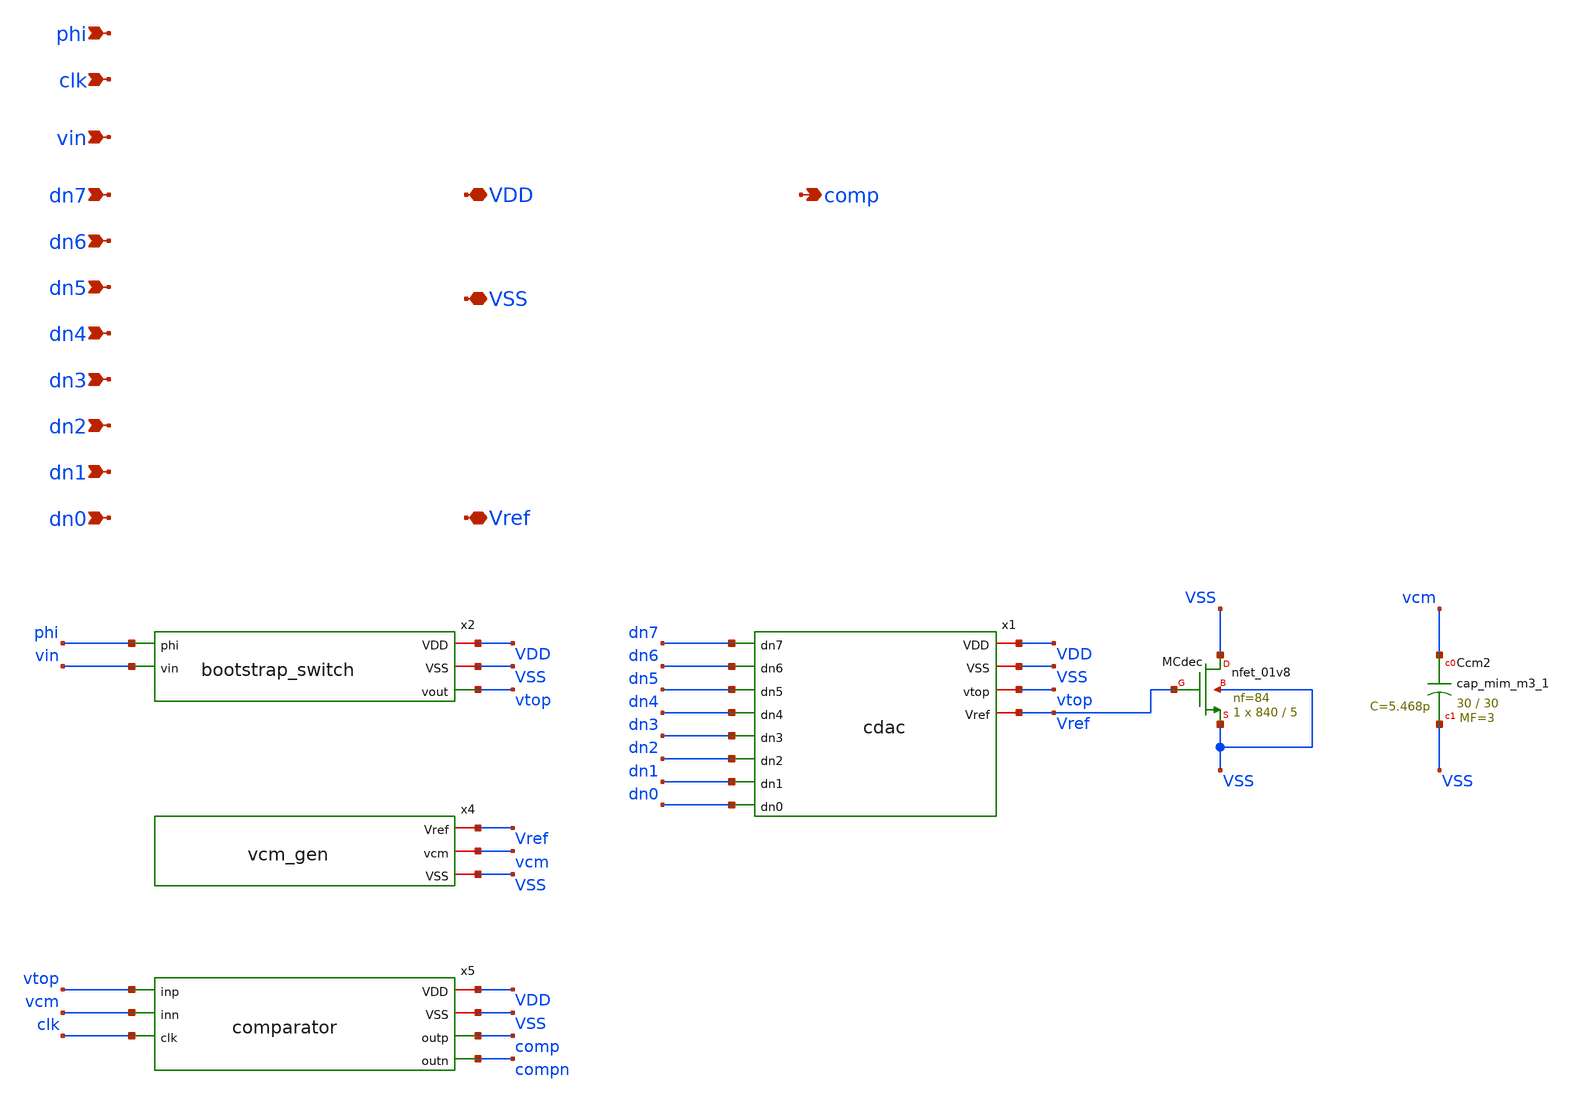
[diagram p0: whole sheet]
** sch_path: xschem/adc_core.sch
**.subckt adc_core dn7 dn6 dn5 dn4 dn3 dn2 dn1 dn0 VDD VSS Vref comp phi clk vin
*.ipin dn7
*.ipin dn6
*.ipin dn5
*.ipin dn4
*.ipin dn3
*.ipin dn2
*.ipin dn1
*.ipin dn0
*.iopin VDD
*.iopin VSS
*.iopin Vref
*.opin comp
*.ipin phi
*.ipin clk
*.ipin vin
x2 phi VDD VSS vin vtop bootstrap_switch
x4 Vref vcm VSS vcm_gen
x1 VDD dn7 dn6 dn5 VSS dn4 dn3 vtop dn2 dn1 Vref dn0 cdac
x5 vtop VDD vcm clk VSS comp compn comparator
XMCdec VSS Vref VSS VSS sky130_fd_pr__nfet_01v8 L=5 W=840 nf=84 ad='int((84 + 1)/2) * 840 / 84 * 0.29'
+ as='int((84 + 2)/2) * 840 / 84 * 0.29' pd='2*int((84 + 1)/2) * (840 / 84 + 0.29)' ps='2*int((84 + 2)/2) * (840 / 84 + 0.29)'
+ nrd='0.29 / 840 ' nrs='0.29 / 840 ' sa=0 sb=0 sd=0 mult=1 m=1
XCcm2 vcm VSS sky130_fd_pr__cap_mim_m3_1 W=30 L=30 MF=3 m=3
**.ends

* expanding   symbol:  bootstrap_switch.sym # of pins=5
** sym_path: xschem/bootstrap_switch.sym
** sch_path: xschem/bootstrap_switch.sch
.subckt bootstrap_switch phi VDD VSS vin vout
*.iopin VDD
*.iopin VSS
*.opin vout
*.ipin phi
*.ipin vin
XM8 X N P P sky130_fd_pr__pfet_01v8 L=0.15 W=2 nf=1 ad='int((1 + 1)/2) * 2 / 1 * 0.29' as='int((1 + 2)/2) * 2 / 1 * 0.29'
+ pd='2*int((1 + 1)/2) * (2 / 1 + 0.29)' ps='2*int((1 + 2)/2) * (2 / 1 + 0.29)' nrd='0.29 / 2 ' nrs='0.29 / 2 '
+ sa=0 sb=0 sd=0 mult=1 m=1
XM11 vin X vout VSS sky130_fd_pr__nfet_01v8 L=0.15 W=1 nf=1 ad='int((1 + 1)/2) * 1 / 1 * 0.29' as='int((1 + 2)/2) * 1 / 1 * 0.29'
+ pd='2*int((1 + 1)/2) * (1 / 1 + 0.29)' ps='2*int((1 + 2)/2) * (1 / 1 + 0.29)' nrd='0.29 / 1 ' nrs='0.29 / 1 '
+ sa=0 sb=0 sd=0 mult=1 m=1
XC2 P B sky130_fd_pr__cap_mim_m3_1 W=11 L=11 MF=2 m=2
XM9 B X vin VSS sky130_fd_pr__nfet_01v8 L=0.15 W=2 nf=1 ad='int((1 + 1)/2) * 2 / 1 * 0.29' as='int((1 + 2)/2) * 2 / 1 * 0.29'
+ pd='2*int((1 + 1)/2) * (2 / 1 + 0.29)' ps='2*int((1 + 2)/2) * (2 / 1 + 0.29)' nrd='0.29 / 2 ' nrs='0.29 / 2 '
+ sa=0 sb=0 sd=0 mult=1 m=1
XM12 VSS phi_b B VSS sky130_fd_pr__nfet_01v8 L=0.15 W=1 nf=1 ad='int((1 + 1)/2) * 1 / 1 * 0.29' as='int((1 + 2)/2) * 1 / 1 * 0.29'
+ pd='2*int((1 + 1)/2) * (1 / 1 + 0.29)' ps='2*int((1 + 2)/2) * (1 / 1 + 0.29)' nrd='0.29 / 1 ' nrs='0.29 / 1 '
+ sa=0 sb=0 sd=0 mult=1 m=1
XM14 X VDD net1 VSS sky130_fd_pr__nfet_01v8 L=0.15 W=4 nf=1 ad='int((1 + 1)/2) * 4 / 1 * 0.29' as='int((1 + 2)/2) * 4 / 1 * 0.29'
+ pd='2*int((1 + 1)/2) * (4 / 1 + 0.29)' ps='2*int((1 + 2)/2) * (4 / 1 + 0.29)' nrd='0.29 / 4 ' nrs='0.29 / 4 '
+ sa=0 sb=0 sd=0 mult=1 m=1
XM3 P X VDD P sky130_fd_pr__pfet_01v8 L=0.15 W=2 nf=1 ad='int((1 + 1)/2) * 2 / 1 * 0.29' as='int((1 + 2)/2) * 2 / 1 * 0.29'
+ pd='2*int((1 + 1)/2) * (2 / 1 + 0.29)' ps='2*int((1 + 2)/2) * (2 / 1 + 0.29)' nrd='0.29 / 2 ' nrs='0.29 / 2 '
+ sa=0 sb=0 sd=0 mult=1 m=1
XM10 net1 phi_b VSS VSS sky130_fd_pr__nfet_01v8 L=0.15 W=1 nf=1 ad='int((1 + 1)/2) * 1 / 1 * 0.29' as='int((1 + 2)/2) * 1 / 1 * 0.29'
+ pd='2*int((1 + 1)/2) * (1 / 1 + 0.29)' ps='2*int((1 + 2)/2) * (1 / 1 + 0.29)' nrd='0.29 / 1 ' nrs='0.29 / 1 '
+ sa=0 sb=0 sd=0 mult=1 m=1
XM15 N phi B VSS sky130_fd_pr__nfet_01v8 L=0.15 W=1 nf=1 ad='int((1 + 1)/2) * 1 / 1 * 0.29' as='int((1 + 2)/2) * 1 / 1 * 0.29'
+ pd='2*int((1 + 1)/2) * (1 / 1 + 0.29)' ps='2*int((1 + 2)/2) * (1 / 1 + 0.29)' nrd='0.29 / 1 ' nrs='0.29 / 1 '
+ sa=0 sb=0 sd=0 mult=1 m=1
XM16 N phi VDD VDD sky130_fd_pr__pfet_01v8 L=0.15 W=1 nf=1 ad='int((1 + 1)/2) * 1 / 1 * 0.29' as='int((1 + 2)/2) * 1 / 1 * 0.29'
+ pd='2*int((1 + 1)/2) * (1 / 1 + 0.29)' ps='2*int((1 + 2)/2) * (1 / 1 + 0.29)' nrd='0.29 / 1 ' nrs='0.29 / 1 '
+ sa=0 sb=0 sd=0 mult=1 m=1
XMIN phi_b phi VSS VSS sky130_fd_pr__nfet_01v8 L=0.15 W=1 nf=1 ad='int((1 + 1)/2) * 1 / 1 * 0.29' as='int((1 + 2)/2) * 1 / 1 * 0.29'
+ pd='2*int((1 + 1)/2) * (1 / 1 + 0.29)' ps='2*int((1 + 2)/2) * (1 / 1 + 0.29)' nrd='0.29 / 1 ' nrs='0.29 / 1 '
+ sa=0 sb=0 sd=0 mult=1 m=1
XMIP phi_b phi VDD VDD sky130_fd_pr__pfet_01v8 L=0.15 W=2 nf=1 ad='int((1 + 1)/2) * 2 / 1 * 0.29' as='int((1 + 2)/2) * 2 / 1 * 0.29'
+ pd='2*int((1 + 1)/2) * (2 / 1 + 0.29)' ps='2*int((1 + 2)/2) * (2 / 1 + 0.29)' nrd='0.29 / 2 ' nrs='0.29 / 2 '
+ sa=0 sb=0 sd=0 mult=1 m=1
.ends


* expanding   symbol:  vcm_gen.sym # of pins=3
** sym_path: xschem/vcm_gen.sym
** sch_path: xschem/vcm_gen.sch
.subckt vcm_gen Vref vcm VSS
*.iopin Vref
*.iopin vcm
*.iopin VSS
XR1 vcm Vref VSS sky130_fd_pr__res_xhigh_po_0p35 L=9 mult=1 m=1
XR2 VSS vcm VSS sky130_fd_pr__res_xhigh_po_0p35 L=9 mult=1 m=1
XCcm vcm VSS sky130_fd_pr__cap_mim_m3_1 W=22 L=22 MF=2 m=2
.ends


* expanding   symbol:  cdac.sym # of pins=12
** sym_path: xschem/cdac.sym
** sch_path: xschem/cdac.sch
.subckt cdac VDD dn7 dn6 dn5 VSS dn4 dn3 vtop dn2 dn1 Vref dn0
*.ipin dn7
*.ipin dn6
*.ipin dn5
*.ipin dn4
*.ipin dn3
*.ipin dn2
*.ipin dn1
*.ipin dn0
*.iopin VDD
*.iopin VSS
*.iopin vtop
*.iopin Vref
XMN7 b7 dn7 VSS VSS sky130_fd_pr__nfet_01v8 L=0.15 W=16 nf=4 ad='int((4 + 1)/2) * 16 / 4 * 0.29' as='int((4 + 2)/2) * 16 / 4 * 0.29'
+ pd='2*int((4 + 1)/2) * (16 / 4 + 0.29)' ps='2*int((4 + 2)/2) * (16 / 4 + 0.29)' nrd='0.29 / 16 ' nrs='0.29 / 16 '
+ sa=0 sb=0 sd=0 mult=1 m=1
XMP7 b7 dn7 Vref Vref sky130_fd_pr__pfet_01v8_lvt L=0.35 W=32 nf=8 ad='int((8 + 1)/2) * 32 / 8 * 0.29'
+ as='int((8 + 2)/2) * 32 / 8 * 0.29' pd='2*int((8 + 1)/2) * (32 / 8 + 0.29)' ps='2*int((8 + 2)/2) * (32 / 8 + 0.29)'
+ nrd='0.29 / 32 ' nrs='0.29 / 32 ' sa=0 sb=0 sd=0 mult=1 m=1
XC7 vtop b7 sky130_fd_pr__cap_mim_m3_1 W=1.8 L=1.8 MF=128 m=128
XMN6 b6 dn6 VSS VSS sky130_fd_pr__nfet_01v8 L=0.15 W=8 nf=2 ad='int((2 + 1)/2) * 8 / 2 * 0.29' as='int((2 + 2)/2) * 8 / 2 * 0.29'
+ pd='2*int((2 + 1)/2) * (8 / 2 + 0.29)' ps='2*int((2 + 2)/2) * (8 / 2 + 0.29)' nrd='0.29 / 8 ' nrs='0.29 / 8 '
+ sa=0 sb=0 sd=0 mult=1 m=1
XMP6 b6 dn6 Vref Vref sky130_fd_pr__pfet_01v8_lvt L=0.35 W=16 nf=4 ad='int((4 + 1)/2) * 16 / 4 * 0.29'
+ as='int((4 + 2)/2) * 16 / 4 * 0.29' pd='2*int((4 + 1)/2) * (16 / 4 + 0.29)' ps='2*int((4 + 2)/2) * (16 / 4 + 0.29)'
+ nrd='0.29 / 16 ' nrs='0.29 / 16 ' sa=0 sb=0 sd=0 mult=1 m=1
XC6 vtop b6 sky130_fd_pr__cap_mim_m3_1 W=1.8 L=1.8 MF=64 m=64
XMN5 b5 dn5 VSS VSS sky130_fd_pr__nfet_01v8 L=0.15 W=4 nf=1 ad='int((1 + 1)/2) * 4 / 1 * 0.29' as='int((1 + 2)/2) * 4 / 1 * 0.29'
+ pd='2*int((1 + 1)/2) * (4 / 1 + 0.29)' ps='2*int((1 + 2)/2) * (4 / 1 + 0.29)' nrd='0.29 / 4 ' nrs='0.29 / 4 '
+ sa=0 sb=0 sd=0 mult=1 m=1
XMP5 b5 dn5 Vref Vref sky130_fd_pr__pfet_01v8_lvt L=0.35 W=8 nf=2 ad='int((2 + 1)/2) * 8 / 2 * 0.29'
+ as='int((2 + 2)/2) * 8 / 2 * 0.29' pd='2*int((2 + 1)/2) * (8 / 2 + 0.29)' ps='2*int((2 + 2)/2) * (8 / 2 + 0.29)'
+ nrd='0.29 / 8 ' nrs='0.29 / 8 ' sa=0 sb=0 sd=0 mult=1 m=1
XC5 vtop b5 sky130_fd_pr__cap_mim_m3_1 W=1.8 L=1.8 MF=32 m=32
XMN4 b4 dn4 VSS VSS sky130_fd_pr__nfet_01v8 L=0.15 W=2 nf=1 ad='int((1 + 1)/2) * 2 / 1 * 0.29' as='int((1 + 2)/2) * 2 / 1 * 0.29'
+ pd='2*int((1 + 1)/2) * (2 / 1 + 0.29)' ps='2*int((1 + 2)/2) * (2 / 1 + 0.29)' nrd='0.29 / 2 ' nrs='0.29 / 2 '
+ sa=0 sb=0 sd=0 mult=1 m=1
XMP4 b4 dn4 Vref Vref sky130_fd_pr__pfet_01v8_lvt L=0.35 W=4 nf=1 ad='int((1 + 1)/2) * 4 / 1 * 0.29'
+ as='int((1 + 2)/2) * 4 / 1 * 0.29' pd='2*int((1 + 1)/2) * (4 / 1 + 0.29)' ps='2*int((1 + 2)/2) * (4 / 1 + 0.29)'
+ nrd='0.29 / 4 ' nrs='0.29 / 4 ' sa=0 sb=0 sd=0 mult=1 m=1
XC4 vtop b4 sky130_fd_pr__cap_mim_m3_1 W=1.8 L=1.8 MF=16 m=16
XMN3 b3 dn3 VSS VSS sky130_fd_pr__nfet_01v8 L=0.15 W=0.5 nf=1 ad='int((1 + 1)/2) * 0.5 / 1 * 0.29' as='int((1 + 2)/2) * 0.5 / 1 * 0.29'
+ pd='2*int((1 + 1)/2) * (0.5 / 1 + 0.29)' ps='2*int((1 + 2)/2) * (0.5 / 1 + 0.29)' nrd='0.29 / 0.5 ' nrs='0.29 / 0.5 '
+ sa=0 sb=0 sd=0 mult=1 m=1
XMP3 b3 dn3 Vref Vref sky130_fd_pr__pfet_01v8_lvt L=0.35 W=1 nf=1 ad='int((1 + 1)/2) * 1 / 1 * 0.29'
+ as='int((1 + 2)/2) * 1 / 1 * 0.29' pd='2*int((1 + 1)/2) * (1 / 1 + 0.29)' ps='2*int((1 + 2)/2) * (1 / 1 + 0.29)'
+ nrd='0.29 / 1 ' nrs='0.29 / 1 ' sa=0 sb=0 sd=0 mult=1 m=1
XC3 vtop b3 sky130_fd_pr__cap_mim_m3_1 W=1.8 L=1.8 MF=8 m=8
XMN2 b2 dn2 VSS VSS sky130_fd_pr__nfet_01v8 L=0.15 W=0.5 nf=1 ad='int((1 + 1)/2) * 0.5 / 1 * 0.29' as='int((1 + 2)/2) * 0.5 / 1 * 0.29'
+ pd='2*int((1 + 1)/2) * (0.5 / 1 + 0.29)' ps='2*int((1 + 2)/2) * (0.5 / 1 + 0.29)' nrd='0.29 / 0.5 ' nrs='0.29 / 0.5 '
+ sa=0 sb=0 sd=0 mult=1 m=1
XMP2 b2 dn2 Vref Vref sky130_fd_pr__pfet_01v8_lvt L=0.35 W=1 nf=1 ad='int((1 + 1)/2) * 1 / 1 * 0.29'
+ as='int((1 + 2)/2) * 1 / 1 * 0.29' pd='2*int((1 + 1)/2) * (1 / 1 + 0.29)' ps='2*int((1 + 2)/2) * (1 / 1 + 0.29)'
+ nrd='0.29 / 1 ' nrs='0.29 / 1 ' sa=0 sb=0 sd=0 mult=1 m=1
XC2 vtop b2 sky130_fd_pr__cap_mim_m3_1 W=1.8 L=1.8 MF=4 m=4
XMN1 b1 dn1 VSS VSS sky130_fd_pr__nfet_01v8 L=0.15 W=0.5 nf=1 ad='int((1 + 1)/2) * 0.5 / 1 * 0.29' as='int((1 + 2)/2) * 0.5 / 1 * 0.29'
+ pd='2*int((1 + 1)/2) * (0.5 / 1 + 0.29)' ps='2*int((1 + 2)/2) * (0.5 / 1 + 0.29)' nrd='0.29 / 0.5 ' nrs='0.29 / 0.5 '
+ sa=0 sb=0 sd=0 mult=1 m=1
XMP1 b1 dn1 Vref Vref sky130_fd_pr__pfet_01v8_lvt L=0.35 W=1 nf=1 ad='int((1 + 1)/2) * 1 / 1 * 0.29'
+ as='int((1 + 2)/2) * 1 / 1 * 0.29' pd='2*int((1 + 1)/2) * (1 / 1 + 0.29)' ps='2*int((1 + 2)/2) * (1 / 1 + 0.29)'
+ nrd='0.29 / 1 ' nrs='0.29 / 1 ' sa=0 sb=0 sd=0 mult=1 m=1
XC1 vtop b1 sky130_fd_pr__cap_mim_m3_1 W=1.8 L=1.8 MF=2 m=2
XMN0 b0 dn0 VSS VSS sky130_fd_pr__nfet_01v8 L=0.15 W=0.5 nf=1 ad='int((1 + 1)/2) * 0.5 / 1 * 0.29' as='int((1 + 2)/2) * 0.5 / 1 * 0.29'
+ pd='2*int((1 + 1)/2) * (0.5 / 1 + 0.29)' ps='2*int((1 + 2)/2) * (0.5 / 1 + 0.29)' nrd='0.29 / 0.5 ' nrs='0.29 / 0.5 '
+ sa=0 sb=0 sd=0 mult=1 m=1
XMP0 b0 dn0 Vref Vref sky130_fd_pr__pfet_01v8_lvt L=0.35 W=1 nf=1 ad='int((1 + 1)/2) * 1 / 1 * 0.29'
+ as='int((1 + 2)/2) * 1 / 1 * 0.29' pd='2*int((1 + 1)/2) * (1 / 1 + 0.29)' ps='2*int((1 + 2)/2) * (1 / 1 + 0.29)'
+ nrd='0.29 / 1 ' nrs='0.29 / 1 ' sa=0 sb=0 sd=0 mult=1 m=1
XC0 vtop b0 sky130_fd_pr__cap_mim_m3_1 W=1.8 L=1.8 MF=1 m=1
XCdmy vtop VSS sky130_fd_pr__cap_mim_m3_1 W=1.8 L=1.8 MF=1 m=1
.ends


* expanding   symbol:  comparator.sym # of pins=7
** sym_path: xschem/comparator.sym
** sch_path: xschem/comparator.sch
.subckt comparator inp VDD inn clk VSS outp outn
*.ipin inp
*.ipin inn
*.ipin clk
*.opin outp
*.opin outn
*.iopin VDD
*.iopin VSS
x1 inp VDD inn clk VSS X Y comparator_sa
XMI1N Yb Y VSS VSS sky130_fd_pr__nfet_01v8 L=0.15 W=1 nf=1 ad='int((1 + 1)/2) * 1 / 1 * 0.29' as='int((1 + 2)/2) * 1 / 1 * 0.29'
+ pd='2*int((1 + 1)/2) * (1 / 1 + 0.29)' ps='2*int((1 + 2)/2) * (1 / 1 + 0.29)' nrd='0.29 / 1 ' nrs='0.29 / 1 '
+ sa=0 sb=0 sd=0 mult=1 m=1
XMI1P Yb Y VDD VDD sky130_fd_pr__pfet_01v8 L=0.15 W=2 nf=1 ad='int((1 + 1)/2) * 2 / 1 * 0.29' as='int((1 + 2)/2) * 2 / 1 * 0.29'
+ pd='2*int((1 + 1)/2) * (2 / 1 + 0.29)' ps='2*int((1 + 2)/2) * (2 / 1 + 0.29)' nrd='0.29 / 2 ' nrs='0.29 / 2 '
+ sa=0 sb=0 sd=0 mult=1 m=1
XMI2N Xb X VSS VSS sky130_fd_pr__nfet_01v8 L=0.15 W=1 nf=1 ad='int((1 + 1)/2) * 1 / 1 * 0.29' as='int((1 + 2)/2) * 1 / 1 * 0.29'
+ pd='2*int((1 + 1)/2) * (1 / 1 + 0.29)' ps='2*int((1 + 2)/2) * (1 / 1 + 0.29)' nrd='0.29 / 1 ' nrs='0.29 / 1 '
+ sa=0 sb=0 sd=0 mult=1 m=1
XMI2P Xb X VDD VDD sky130_fd_pr__pfet_01v8 L=0.15 W=2 nf=1 ad='int((1 + 1)/2) * 2 / 1 * 0.29' as='int((1 + 2)/2) * 2 / 1 * 0.29'
+ pd='2*int((1 + 1)/2) * (2 / 1 + 0.29)' ps='2*int((1 + 2)/2) * (2 / 1 + 0.29)' nrd='0.29 / 2 ' nrs='0.29 / 2 '
+ sa=0 sb=0 sd=0 mult=1 m=1
XMA1 outp Yb VDD VDD sky130_fd_pr__pfet_01v8 L=0.15 W=1 nf=1 ad='int((1 + 1)/2) * 1 / 1 * 0.29' as='int((1 + 2)/2) * 1 / 1 * 0.29'
+ pd='2*int((1 + 1)/2) * (1 / 1 + 0.29)' ps='2*int((1 + 2)/2) * (1 / 1 + 0.29)' nrd='0.29 / 1 ' nrs='0.29 / 1 '
+ sa=0 sb=0 sd=0 mult=1 m=1
XMA2 outp outn VDD VDD sky130_fd_pr__pfet_01v8 L=0.15 W=1 nf=1 ad='int((1 + 1)/2) * 1 / 1 * 0.29' as='int((1 + 2)/2) * 1 / 1 * 0.29'
+ pd='2*int((1 + 1)/2) * (1 / 1 + 0.29)' ps='2*int((1 + 2)/2) * (1 / 1 + 0.29)' nrd='0.29 / 1 ' nrs='0.29 / 1 '
+ sa=0 sb=0 sd=0 mult=1 m=1
XMA3 outp Yb na VSS sky130_fd_pr__nfet_01v8 L=0.15 W=2 nf=1 ad='int((1 + 1)/2) * 2 / 1 * 0.29' as='int((1 + 2)/2) * 2 / 1 * 0.29'
+ pd='2*int((1 + 1)/2) * (2 / 1 + 0.29)' ps='2*int((1 + 2)/2) * (2 / 1 + 0.29)' nrd='0.29 / 2 ' nrs='0.29 / 2 '
+ sa=0 sb=0 sd=0 mult=1 m=1
XMA4 na outn VSS VSS sky130_fd_pr__nfet_01v8 L=0.15 W=2 nf=1 ad='int((1 + 1)/2) * 2 / 1 * 0.29' as='int((1 + 2)/2) * 2 / 1 * 0.29'
+ pd='2*int((1 + 1)/2) * (2 / 1 + 0.29)' ps='2*int((1 + 2)/2) * (2 / 1 + 0.29)' nrd='0.29 / 2 ' nrs='0.29 / 2 '
+ sa=0 sb=0 sd=0 mult=1 m=1
XMB1 outn Xb VDD VDD sky130_fd_pr__pfet_01v8 L=0.15 W=1 nf=1 ad='int((1 + 1)/2) * 1 / 1 * 0.29' as='int((1 + 2)/2) * 1 / 1 * 0.29'
+ pd='2*int((1 + 1)/2) * (1 / 1 + 0.29)' ps='2*int((1 + 2)/2) * (1 / 1 + 0.29)' nrd='0.29 / 1 ' nrs='0.29 / 1 '
+ sa=0 sb=0 sd=0 mult=1 m=1
XMB2 outn outp VDD VDD sky130_fd_pr__pfet_01v8 L=0.15 W=1 nf=1 ad='int((1 + 1)/2) * 1 / 1 * 0.29' as='int((1 + 2)/2) * 1 / 1 * 0.29'
+ pd='2*int((1 + 1)/2) * (1 / 1 + 0.29)' ps='2*int((1 + 2)/2) * (1 / 1 + 0.29)' nrd='0.29 / 1 ' nrs='0.29 / 1 '
+ sa=0 sb=0 sd=0 mult=1 m=1
XMB3 outn Xb nb VSS sky130_fd_pr__nfet_01v8 L=0.15 W=2 nf=1 ad='int((1 + 1)/2) * 2 / 1 * 0.29' as='int((1 + 2)/2) * 2 / 1 * 0.29'
+ pd='2*int((1 + 1)/2) * (2 / 1 + 0.29)' ps='2*int((1 + 2)/2) * (2 / 1 + 0.29)' nrd='0.29 / 2 ' nrs='0.29 / 2 '
+ sa=0 sb=0 sd=0 mult=1 m=1
XMB4 nb outp VSS VSS sky130_fd_pr__nfet_01v8 L=0.15 W=2 nf=1 ad='int((1 + 1)/2) * 2 / 1 * 0.29' as='int((1 + 2)/2) * 2 / 1 * 0.29'
+ pd='2*int((1 + 1)/2) * (2 / 1 + 0.29)' ps='2*int((1 + 2)/2) * (2 / 1 + 0.29)' nrd='0.29 / 2 ' nrs='0.29 / 2 '
+ sa=0 sb=0 sd=0 mult=1 m=1
.ends


* expanding   symbol:  comparator_sa.sym # of pins=7
** sym_path: xschem/comparator_sa.sym
** sch_path: xschem/comparator_sa.sch
.subckt comparator_sa inp VDD inn clk VSS X Y
*.ipin inp
*.ipin inn
*.ipin clk
*.opin X
*.opin Y
*.iopin VDD
*.iopin VSS
XM7 T ckb VDD VDD sky130_fd_pr__pfet_01v8 L=0.15 W=4 nf=1 ad='int((1 + 1)/2) * 4 / 1 * 0.29' as='int((1 + 2)/2) * 4 / 1 * 0.29'
+ pd='2*int((1 + 1)/2) * (4 / 1 + 0.29)' ps='2*int((1 + 2)/2) * (4 / 1 + 0.29)' nrd='0.29 / 4 ' nrs='0.29 / 4 '
+ sa=0 sb=0 sd=0 mult=1 m=1
XM1 P inp T T sky130_fd_pr__pfet_01v8 L=0.5 W=8 nf=4 ad='int((4 + 1)/2) * 8 / 4 * 0.29' as='int((4 + 2)/2) * 8 / 4 * 0.29'
+ pd='2*int((4 + 1)/2) * (8 / 4 + 0.29)' ps='2*int((4 + 2)/2) * (8 / 4 + 0.29)' nrd='0.29 / 8 ' nrs='0.29 / 8 '
+ sa=0 sb=0 sd=0 mult=1 m=1
XM2 Q inn T T sky130_fd_pr__pfet_01v8 L=0.5 W=8 nf=4 ad='int((4 + 1)/2) * 8 / 4 * 0.29' as='int((4 + 2)/2) * 8 / 4 * 0.29'
+ pd='2*int((4 + 1)/2) * (8 / 4 + 0.29)' ps='2*int((4 + 2)/2) * (8 / 4 + 0.29)' nrd='0.29 / 8 ' nrs='0.29 / 8 '
+ sa=0 sb=0 sd=0 mult=1 m=1
XM3 X Y P VDD sky130_fd_pr__pfet_01v8 L=0.15 W=2 nf=1 ad='int((1 + 1)/2) * 2 / 1 * 0.29' as='int((1 + 2)/2) * 2 / 1 * 0.29'
+ pd='2*int((1 + 1)/2) * (2 / 1 + 0.29)' ps='2*int((1 + 2)/2) * (2 / 1 + 0.29)' nrd='0.29 / 2 ' nrs='0.29 / 2 '
+ sa=0 sb=0 sd=0 mult=1 m=1
XM4 Y X Q VDD sky130_fd_pr__pfet_01v8 L=0.15 W=2 nf=1 ad='int((1 + 1)/2) * 2 / 1 * 0.29' as='int((1 + 2)/2) * 2 / 1 * 0.29'
+ pd='2*int((1 + 1)/2) * (2 / 1 + 0.29)' ps='2*int((1 + 2)/2) * (2 / 1 + 0.29)' nrd='0.29 / 2 ' nrs='0.29 / 2 '
+ sa=0 sb=0 sd=0 mult=1 m=1
XM6 Y X VSS VSS sky130_fd_pr__nfet_01v8 L=0.15 W=1 nf=1 ad='int((1 + 1)/2) * 1 / 1 * 0.29' as='int((1 + 2)/2) * 1 / 1 * 0.29'
+ pd='2*int((1 + 1)/2) * (1 / 1 + 0.29)' ps='2*int((1 + 2)/2) * (1 / 1 + 0.29)' nrd='0.29 / 1 ' nrs='0.29 / 1 '
+ sa=0 sb=0 sd=0 mult=1 m=1
XM5 X Y VSS VSS sky130_fd_pr__nfet_01v8 L=0.15 W=1 nf=1 ad='int((1 + 1)/2) * 1 / 1 * 0.29' as='int((1 + 2)/2) * 1 / 1 * 0.29'
+ pd='2*int((1 + 1)/2) * (1 / 1 + 0.29)' ps='2*int((1 + 2)/2) * (1 / 1 + 0.29)' nrd='0.29 / 1 ' nrs='0.29 / 1 '
+ sa=0 sb=0 sd=0 mult=1 m=1
XS4 Y ckb VSS VSS sky130_fd_pr__nfet_01v8 L=0.6 W=2 nf=1 ad='int((1 + 1)/2) * 2 / 1 * 0.29' as='int((1 + 2)/2) * 2 / 1 * 0.29'
+ pd='2*int((1 + 1)/2) * (2 / 1 + 0.29)' ps='2*int((1 + 2)/2) * (2 / 1 + 0.29)' nrd='0.29 / 2 ' nrs='0.29 / 2 '
+ sa=0 sb=0 sd=0 mult=1 m=1
XS2 Q ckb VSS VSS sky130_fd_pr__nfet_01v8 L=0.6 W=2 nf=1 ad='int((1 + 1)/2) * 2 / 1 * 0.29' as='int((1 + 2)/2) * 2 / 1 * 0.29'
+ pd='2*int((1 + 1)/2) * (2 / 1 + 0.29)' ps='2*int((1 + 2)/2) * (2 / 1 + 0.29)' nrd='0.29 / 2 ' nrs='0.29 / 2 '
+ sa=0 sb=0 sd=0 mult=1 m=1
XS3 X ckb VSS VSS sky130_fd_pr__nfet_01v8 L=0.6 W=2 nf=1 ad='int((1 + 1)/2) * 2 / 1 * 0.29' as='int((1 + 2)/2) * 2 / 1 * 0.29'
+ pd='2*int((1 + 1)/2) * (2 / 1 + 0.29)' ps='2*int((1 + 2)/2) * (2 / 1 + 0.29)' nrd='0.29 / 2 ' nrs='0.29 / 2 '
+ sa=0 sb=0 sd=0 mult=1 m=1
XS1 P ckb VSS VSS sky130_fd_pr__nfet_01v8 L=0.6 W=2 nf=1 ad='int((1 + 1)/2) * 2 / 1 * 0.29' as='int((1 + 2)/2) * 2 / 1 * 0.29'
+ pd='2*int((1 + 1)/2) * (2 / 1 + 0.29)' ps='2*int((1 + 2)/2) * (2 / 1 + 0.29)' nrd='0.29 / 2 ' nrs='0.29 / 2 '
+ sa=0 sb=0 sd=0 mult=1 m=1
XMIN ckb clk VSS VSS sky130_fd_pr__nfet_01v8 L=0.15 W=1 nf=1 ad='int((1 + 1)/2) * 1 / 1 * 0.29' as='int((1 + 2)/2) * 1 / 1 * 0.29'
+ pd='2*int((1 + 1)/2) * (1 / 1 + 0.29)' ps='2*int((1 + 2)/2) * (1 / 1 + 0.29)' nrd='0.29 / 1 ' nrs='0.29 / 1 '
+ sa=0 sb=0 sd=0 mult=1 m=1
XMIP ckb clk VDD VDD sky130_fd_pr__pfet_01v8 L=0.15 W=2 nf=1 ad='int((1 + 1)/2) * 2 / 1 * 0.29' as='int((1 + 2)/2) * 2 / 1 * 0.29'
+ pd='2*int((1 + 1)/2) * (2 / 1 + 0.29)' ps='2*int((1 + 2)/2) * (2 / 1 + 0.29)' nrd='0.29 / 2 ' nrs='0.29 / 2 '
+ sa=0 sb=0 sd=0 mult=1 m=1
.ends

.end
